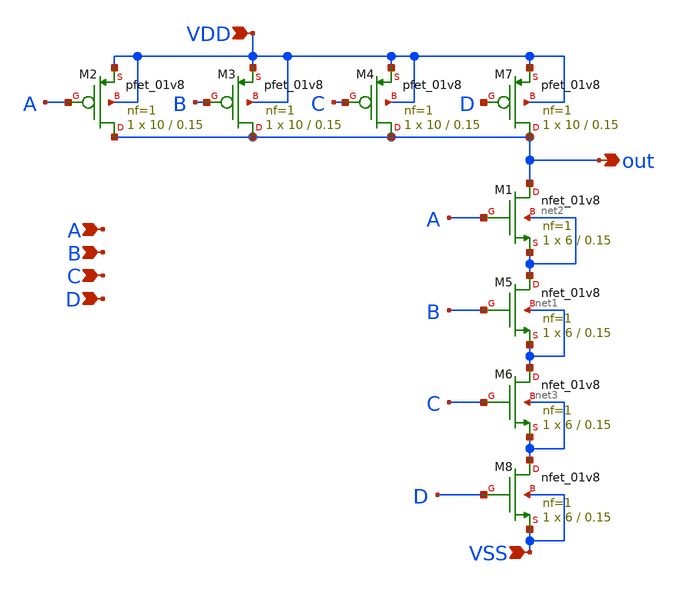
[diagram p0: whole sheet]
** sch_path: nand/nand4.sch
**.subckt nand4 A B C VSS VDD out D
*.ipin A
*.ipin B
*.ipin C
*.ipin VSS
*.ipin VDD
*.opin out
*.ipin D
XM1 out A net2 net2 sky130_fd_pr__nfet_01v8 L=0.15 W=6 nf=1 ad='int((nf+1)/2) * W/nf * 0.29' as='int((nf+2)/2) * W/nf * 0.29'
+ pd='2*int((nf+1)/2) * (W/nf + 0.29)' ps='2*int((nf+2)/2) * (W/nf + 0.29)' nrd='0.29 / W' nrs='0.29 / W'
+ sa=0 sb=0 sd=0 mult=1 m=1
XM2 out A VDD VDD sky130_fd_pr__pfet_01v8 L=0.15 W=10 nf=1 ad='int((nf+1)/2) * W/nf * 0.29' as='int((nf+2)/2) * W/nf * 0.29'
+ pd='2*int((nf+1)/2) * (W/nf + 0.29)' ps='2*int((nf+2)/2) * (W/nf + 0.29)' nrd='0.29 / W' nrs='0.29 / W'
+ sa=0 sb=0 sd=0 mult=1 m=1
XM3 out B VDD VDD sky130_fd_pr__pfet_01v8 L=0.15 W=10 nf=1 ad='int((nf+1)/2) * W/nf * 0.29' as='int((nf+2)/2) * W/nf * 0.29'
+ pd='2*int((nf+1)/2) * (W/nf + 0.29)' ps='2*int((nf+2)/2) * (W/nf + 0.29)' nrd='0.29 / W' nrs='0.29 / W'
+ sa=0 sb=0 sd=0 mult=1 m=1
XM4 out C VDD VDD sky130_fd_pr__pfet_01v8 L=0.15 W=10 nf=1 ad='int((nf+1)/2) * W/nf * 0.29' as='int((nf+2)/2) * W/nf * 0.29'
+ pd='2*int((nf+1)/2) * (W/nf + 0.29)' ps='2*int((nf+2)/2) * (W/nf + 0.29)' nrd='0.29 / W' nrs='0.29 / W'
+ sa=0 sb=0 sd=0 mult=1 m=1
XM5 net2 B net1 net1 sky130_fd_pr__nfet_01v8 L=0.15 W=6 nf=1 ad='int((nf+1)/2) * W/nf * 0.29' as='int((nf+2)/2) * W/nf * 0.29'
+ pd='2*int((nf+1)/2) * (W/nf + 0.29)' ps='2*int((nf+2)/2) * (W/nf + 0.29)' nrd='0.29 / W' nrs='0.29 / W'
+ sa=0 sb=0 sd=0 mult=1 m=1
XM6 net1 C net3 net3 sky130_fd_pr__nfet_01v8 L=0.15 W=6 nf=1 ad='int((nf+1)/2) * W/nf * 0.29' as='int((nf+2)/2) * W/nf * 0.29'
+ pd='2*int((nf+1)/2) * (W/nf + 0.29)' ps='2*int((nf+2)/2) * (W/nf + 0.29)' nrd='0.29 / W' nrs='0.29 / W'
+ sa=0 sb=0 sd=0 mult=1 m=1
XM7 out D VDD VDD sky130_fd_pr__pfet_01v8 L=0.15 W=10 nf=1 ad='int((nf+1)/2) * W/nf * 0.29' as='int((nf+2)/2) * W/nf * 0.29'
+ pd='2*int((nf+1)/2) * (W/nf + 0.29)' ps='2*int((nf+2)/2) * (W/nf + 0.29)' nrd='0.29 / W' nrs='0.29 / W'
+ sa=0 sb=0 sd=0 mult=1 m=1
XM8 net3 D VSS VSS sky130_fd_pr__nfet_01v8 L=0.15 W=6 nf=1 ad='int((nf+1)/2) * W/nf * 0.29' as='int((nf+2)/2) * W/nf * 0.29'
+ pd='2*int((nf+1)/2) * (W/nf + 0.29)' ps='2*int((nf+2)/2) * (W/nf + 0.29)' nrd='0.29 / W' nrs='0.29 / W'
+ sa=0 sb=0 sd=0 mult=1 m=1
**.ends
.end
